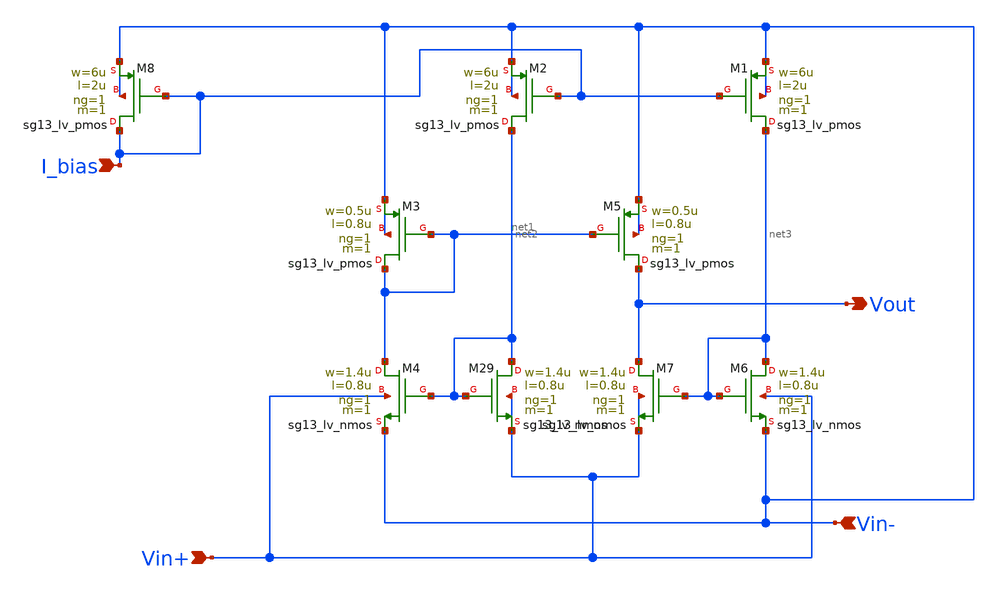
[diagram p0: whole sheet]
** sch_path: SSDOR_1.2V_v2/components/pmos_comp/nmos_comp.sch
**.subckt nmos_comp Vin- Vin+ Vout I_bias
*.ipin Vin-
*.ipin Vin+
*.opin Vout
*.ipin I_bias
XM29 net2 net2 Vin+ Vin+ sg13_lv_nmos w=1.4u l=0.8u ng=1 m=1 mm_ok=1
XM5 Vout net1 Vin- Vin- sg13_lv_pmos w=0.5u l=0.8u ng=1 m=1 mm_ok=1
XM1 net3 I_bias Vin- Vin- sg13_lv_pmos w=6u l=2u ng=1 m=1 mm_ok=1
XM2 net2 I_bias Vin- Vin- sg13_lv_pmos w=6u l=2u ng=1 m=1 mm_ok=1
XM3 net1 net1 Vin- Vin- sg13_lv_pmos w=0.5u l=0.8u ng=1 m=1 mm_ok=1
XM4 net1 net2 Vin- Vin+ sg13_lv_nmos w=1.4u l=0.8u ng=1 m=1 mm_ok=1
XM6 net3 net3 Vin- Vin+ sg13_lv_nmos w=1.4u l=0.8u ng=1 m=1 mm_ok=1
XM7 Vout net3 Vin+ Vin+ sg13_lv_nmos w=1.4u l=0.8u ng=1 m=1 mm_ok=1
XM8 I_bias I_bias Vin- Vin- sg13_lv_pmos w=6u l=2u ng=1 m=1 mm_ok=1
**.ends
.end
